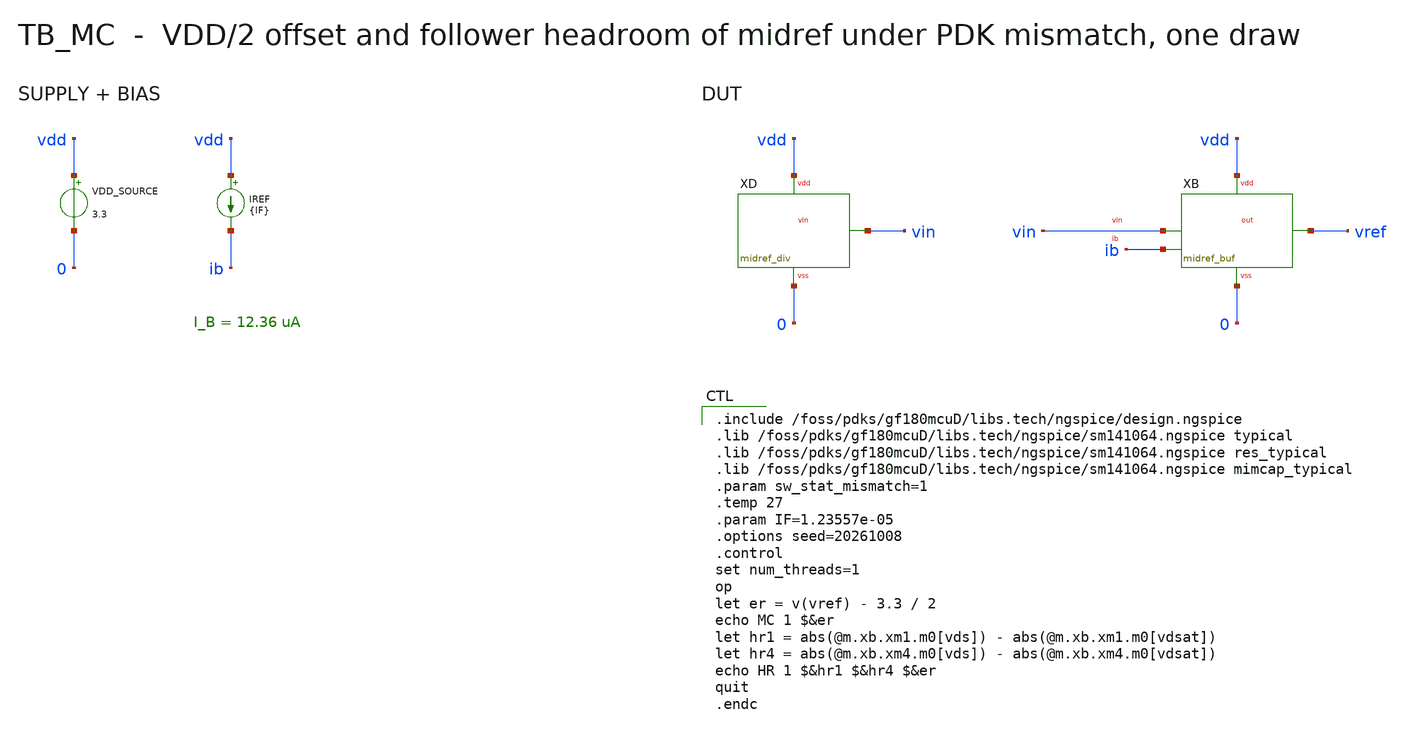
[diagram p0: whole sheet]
** sch_path: mixed_signal/midrail_ref/tb_mc.sch
**.subckt tb_mc
VDD_SOURCE vdd 0 3.3
IREF vdd ib {IF}
XD vin vdd 0 midref_div
XB vref vin ib vdd 0 midref_buf
**** begin user architecture code

.include /foss/pdks/gf180mcuD/libs.tech/ngspice/design.ngspice
.lib /foss/pdks/gf180mcuD/libs.tech/ngspice/sm141064.ngspice typical
.lib /foss/pdks/gf180mcuD/libs.tech/ngspice/sm141064.ngspice res_typical
.lib /foss/pdks/gf180mcuD/libs.tech/ngspice/sm141064.ngspice mimcap_typical
.param sw_stat_mismatch=1
.temp 27
.param IF=1.23557e-05
.options seed=20261008
.control
set num_threads=1
op
let er = v(vref) - 3.3 / 2
echo MC 1 $&er
let hr1 = abs(@m.xb.xm1.m0[vds]) - abs(@m.xb.xm1.m0[vdsat])
let hr4 = abs(@m.xb.xm4.m0[vds]) - abs(@m.xb.xm4.m0[vdsat])
echo HR 1 $&hr1 $&hr4 $&er
quit
.endc

**** end user architecture code
**.ends
.end
